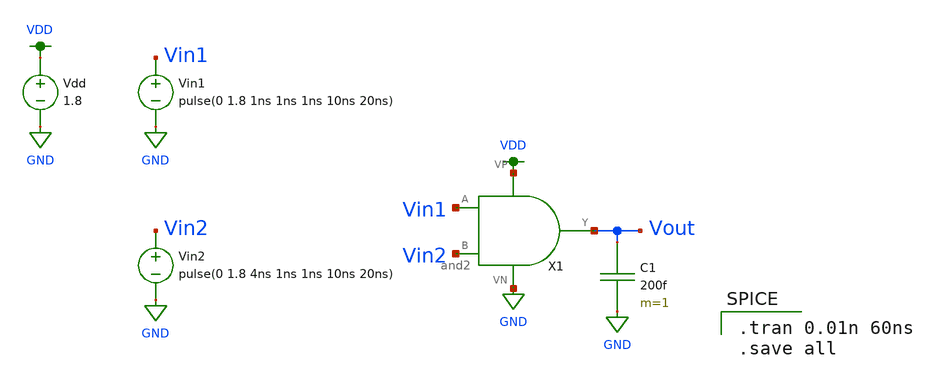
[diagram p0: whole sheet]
** sch_path: and2_tran.sch
**.subckt and2_tran
Vdd VDD GND 1.8
C1 Vout GND 200f m=1
Vin1 Vin1 GND pulse(0 1.8 1ns 1ns 1ns 10ns 20ns)
Vin2 Vin2 GND pulse(0 1.8 4ns 1ns 1ns 10ns 20ns)
X1 Vin2 Vin1 VDD GND Vout and2
**** begin user architecture code

.option wnflag=1
.lib ~/skywater/skywater-pdk/libraries/sky130_fd_pr_ngspice/latest/models/sky130.lib.spice tt


.tran 0.01n 60ns
.save all

**** end user architecture code
**.ends

* expanding   symbol:  /home/madvlsi/Documents/mp1/and2.sym # of pins=5
** sym_path: and2.sym
** sch_path: and2.sch
.subckt and2 B A VP VN Y
*.ipin A
*.ipin B
*.iopin VP
*.iopin VN
*.opin Y
X1 B A net1 VP VN nand2
X2 net1 Y VP VN inverter
.ends


* expanding   symbol:  /home/madvlsi/Documents/mp1/nand2.sym # of pins=5
** sym_path: nand2.sym
** sch_path: nand2.sch
.subckt nand2 B A Y VP VN
*.ipin A
*.ipin B
*.iopin VP
*.iopin VN
*.opin Y
XM1 Y A net1 VN sky130_fd_pr__nfet_01v8 L=0.15 W=1 nf=1 ad='int((nf+1)/2) * W/nf * 0.29' as='int((nf+2)/2) * W/nf * 0.29'
+ pd='2*int((nf+1)/2) * (W/nf + 0.29)' ps='2*int((nf+2)/2) * (W/nf + 0.29)' nrd='0.29 / W' nrs='0.29 / W'
+ sa=0 sb=0 sd=0 mult=1 m=1
XM2 net1 B VN VN sky130_fd_pr__nfet_01v8 L=0.15 W=1 nf=1 ad='int((nf+1)/2) * W/nf * 0.29' as='int((nf+2)/2) * W/nf * 0.29'
+ pd='2*int((nf+1)/2) * (W/nf + 0.29)' ps='2*int((nf+2)/2) * (W/nf + 0.29)' nrd='0.29 / W' nrs='0.29 / W'
+ sa=0 sb=0 sd=0 mult=1 m=1
XM3 Y A VP VP sky130_fd_pr__pfet_01v8 L=0.15 W=1 nf=1 ad='int((nf+1)/2) * W/nf * 0.29' as='int((nf+2)/2) * W/nf * 0.29'
+ pd='2*int((nf+1)/2) * (W/nf + 0.29)' ps='2*int((nf+2)/2) * (W/nf + 0.29)' nrd='0.29 / W' nrs='0.29 / W'
+ sa=0 sb=0 sd=0 mult=1 m=1
XM4 Y B VP VP sky130_fd_pr__pfet_01v8 L=0.15 W=1 nf=1 ad='int((nf+1)/2) * W/nf * 0.29' as='int((nf+2)/2) * W/nf * 0.29'
+ pd='2*int((nf+1)/2) * (W/nf + 0.29)' ps='2*int((nf+2)/2) * (W/nf + 0.29)' nrd='0.29 / W' nrs='0.29 / W'
+ sa=0 sb=0 sd=0 mult=1 m=1
.ends


* expanding   symbol:  /home/madvlsi/Documents/mp1/inverter.sym # of pins=4
** sym_path: inverter.sym
** sch_path: inverter.sch
.subckt inverter A Y VP VN
*.ipin A
*.iopin VP
*.iopin VN
*.opin Y
XM1 Y A VN VN sky130_fd_pr__nfet_01v8 L=0.15 W=1 nf=1 ad='int((nf+1)/2) * W/nf * 0.29' as='int((nf+2)/2) * W/nf * 0.29'
+ pd='2*int((nf+1)/2) * (W/nf + 0.29)' ps='2*int((nf+2)/2) * (W/nf + 0.29)' nrd='0.29 / W' nrs='0.29 / W'
+ sa=0 sb=0 sd=0 mult=1 m=1
XM2 Y A VP VP sky130_fd_pr__pfet_01v8 L=0.15 W=1 nf=1 ad='int((nf+1)/2) * W/nf * 0.29' as='int((nf+2)/2) * W/nf * 0.29'
+ pd='2*int((nf+1)/2) * (W/nf + 0.29)' ps='2*int((nf+2)/2) * (W/nf + 0.29)' nrd='0.29 / W' nrs='0.29 / W'
+ sa=0 sb=0 sd=0 mult=1 m=1
.ends

.GLOBAL GND
.GLOBAL VDD
.end
